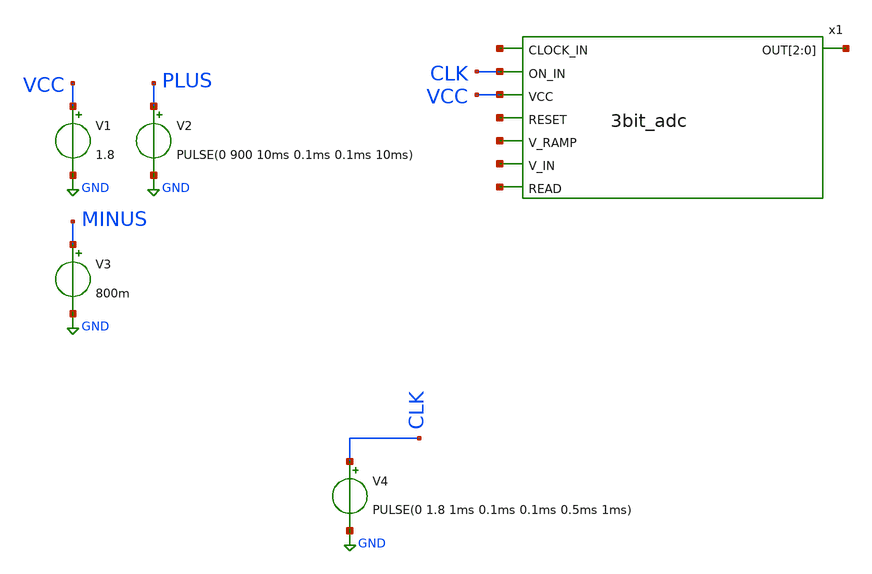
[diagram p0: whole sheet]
** sch_path: xschem/untitled.sch
**.subckt untitled
V1 VCC GND 1.8
V2 PLUS GND PULSE(0 900 10ms 0.1ms 0.1ms 10ms)
V3 MINUS GND 800m
V4 CLK GND PULSE(0 1.8 1ms 0.1ms 0.1ms 0.5ms 1ms)
x1 net1 CLK VCC net2 net3[2] net3[1] net3[0] net4 net5 net6 3bit_adc
**** begin user architecture code

** opencircuitdesign pdks install
.lib $::SKYWATER_MODELS/sky130.lib.spice tt


**** end user architecture code
**.ends

* expanding   symbol:  3bit_adc.sym # of pins=8
** sym_path: xschem/adc/3bit_adc.sym
** sch_path: xschem/adc/3bit_adc.sch
.subckt 3bit_adc CLOCK_IN ON_IN VCC RESET OUT[2] OUT[1] OUT[0] V_RAMP V_IN READ
*.ipin RESET
*.ipin V_IN
*.ipin VCC
*.ipin CLOCK_IN
*.ipin V_RAMP
*.ipin ON_IN
*.ipin READ
*.opin OUT[2],OUT[1],OUT[0]
XM5 net2 GN VCC VCC sky130_fd_pr__pfet_01v8_lvt L=1 W=1 nf=1 ad='W * 0.29' as='W * 0.29' pd='2*(W + 0.29)'
+ ps='2*(W + 0.29)' nrd=0 nrs=0 sa=0 sb=0 sd=0 mult=1 m=1
XM6 GN GN VCC VCC sky130_fd_pr__pfet_01v8_lvt L=1 W=1 nf=1 ad='W * 0.29' as='W * 0.29' pd='2*(W + 0.29)'
+ ps='2*(W + 0.29)' nrd=0 nrs=0 sa=0 sb=0 sd=0 mult=1 m=1
XM23 net2 V_IN SN GND sky130_fd_pr__nfet_01v8_lvt L=0.15 W=1 nf=1 ad='W * 0.29' as='W * 0.29' pd='2*(W + 0.29)'
+ ps='2*(W + 0.29)' nrd=0 nrs=0 sa=0 sb=0 sd=0 mult=1 m=1
XM16 GN V_RAMP SN GND sky130_fd_pr__nfet_01v8_lvt L=0.15 W=1 nf=1 ad='W * 0.29' as='W * 0.29' pd='2*(W + 0.29)'
+ ps='2*(W + 0.29)' nrd=0 nrs=0 sa=0 sb=0 sd=0 mult=1 m=1
I0 SN GND 100n
XM1 ENABLE_D net2 GND GND sky130_fd_pr__nfet_01v8_lvt L=0.15 W=1 nf=1 ad='W * 0.29' as='W * 0.29' pd='2*(W + 0.29)'
+ ps='2*(W + 0.29)' nrd=0 nrs=0 sa=0 sb=0 sd=0 mult=1 m=1
XM2 ENABLE_D net2 VCC VCC sky130_fd_pr__pfet_01v8_lvt L=0.35 W=2 nf=1 ad='W * 0.29' as='W * 0.29' pd='2*(W + 0.29)'
+ ps='2*(W + 0.29)' nrd=0 nrs=0 sa=0 sb=0 sd=0 mult=1 m=1
x12 ON ON_IN adc_bridge
x5 CLOCK CLOCK_IN adc_bridge
x13 RESET_D RESET adc_bridge
x1 ENABLE_D OUT[2] net8 net3 READ dram
x2 ENABLE_D OUT[1] net9 net4 READ dram
x3 ENABLE_D OUT[0] net10 net7 READ dram
x15 net3 net1 dac_bridge
x20 net4 net5 dac_bridge
x21 net7 net6 dac_bridge
x11 ON net1 CLOCK net5 net6 RESET_D 3bit_graycounter
.ends


* expanding   symbol:  digital_prims/adc_bridge.sym # of pins=2
** sym_path: xschem/digital_prims/adc_bridge.sym
** sch_path: xschem/digital_prims/adc_bridge.sch
.subckt adc_bridge D_OUT ANALOG_IN
*.ipin ANALOG_IN
*.opin D_OUT
**** begin user architecture code


abridge [ANALOG_IN] [D_OUT] adc_buff
.model adc_buff adc_bridge(in_low=0.9 in_high =0.9)


**** end user architecture code
.ends


* expanding   symbol:  digital_prims/dram.sym # of pins=5
** sym_path: xschem/digital_prims/dram.sym
** sch_path: xschem/digital_prims/dram.sch
.subckt dram WWL RBL storage WBL RWL
*.opin RBL
*.ipin RWL
*.ipin WBL
*.ipin WWL
*.opin storage
XM3 RWL storage RBL GND sky130_fd_pr__nfet_01v8 L=0.15 W=1 nf=1 ad='int((nf+1)/2) * W/nf * 0.29' as='int((nf+2)/2) * W/nf * 0.29'
+ pd='2*int((nf+1)/2) * (W/nf + 0.29)' ps='2*int((nf+2)/2) * (W/nf + 0.29)' nrd='0.29 / W' nrs='0.29 / W'
+ sa=0 sb=0 sd=0 mult=1 m=1
XM1 WBL WWL storage GND sky130_fd_pr__nfet_01v8 L=0.15 W=1 nf=1 ad='int((nf+1)/2) * W/nf * 0.29' as='int((nf+2)/2) * W/nf * 0.29'
+ pd='2*int((nf+1)/2) * (W/nf + 0.29)' ps='2*int((nf+2)/2) * (W/nf + 0.29)' nrd='0.29 / W' nrs='0.29 / W'
+ sa=0 sb=0 sd=0 mult=1 m=1
.ends


* expanding   symbol:  digital_prims/dac_bridge.sym # of pins=2
** sym_path: xschem/digital_prims/dac_bridge.sym
** sch_path: xschem/digital_prims/dac_bridge.sch
.subckt dac_bridge ANALOG_OUT D_IN
*.ipin D_IN
*.opin ANALOG_OUT
**** begin user architecture code


abridge_d [D_IN] [ANALOG_OUT] dac_buff
.model dac_buff dac_bridge(out_high=1.8)


**** end user architecture code
.ends


* expanding   symbol:  adc/3bit_graycounter.sym # of pins=6
** sym_path: xschem/adc/3bit_graycounter.sym
** sch_path: xschem/adc/3bit_graycounter.sch
.subckt 3bit_graycounter ON_D 1 CLK_D 2 3 RESET
*.ipin ON_D
*.ipin CLK_D
*.ipin RESET
*.opin 1
*.opin 2
*.opin 3
**** begin user architecture code


a1 [ON_D] CLK_D RESET [1 2 3] gc_sm
.model gc_sm d_state(state_file="/home/hni/topmetal_dps/xschem/adc/3bitgray_sm.in")


**** end user architecture code
.ends

.GLOBAL GND
**** begin user architecture code


.control
save all

*dc v2 0 1.8 0.05
*plot v(test)
tran 0.1ms 20ms
plot v(OUT)
.endc


**** end user architecture code
.end
